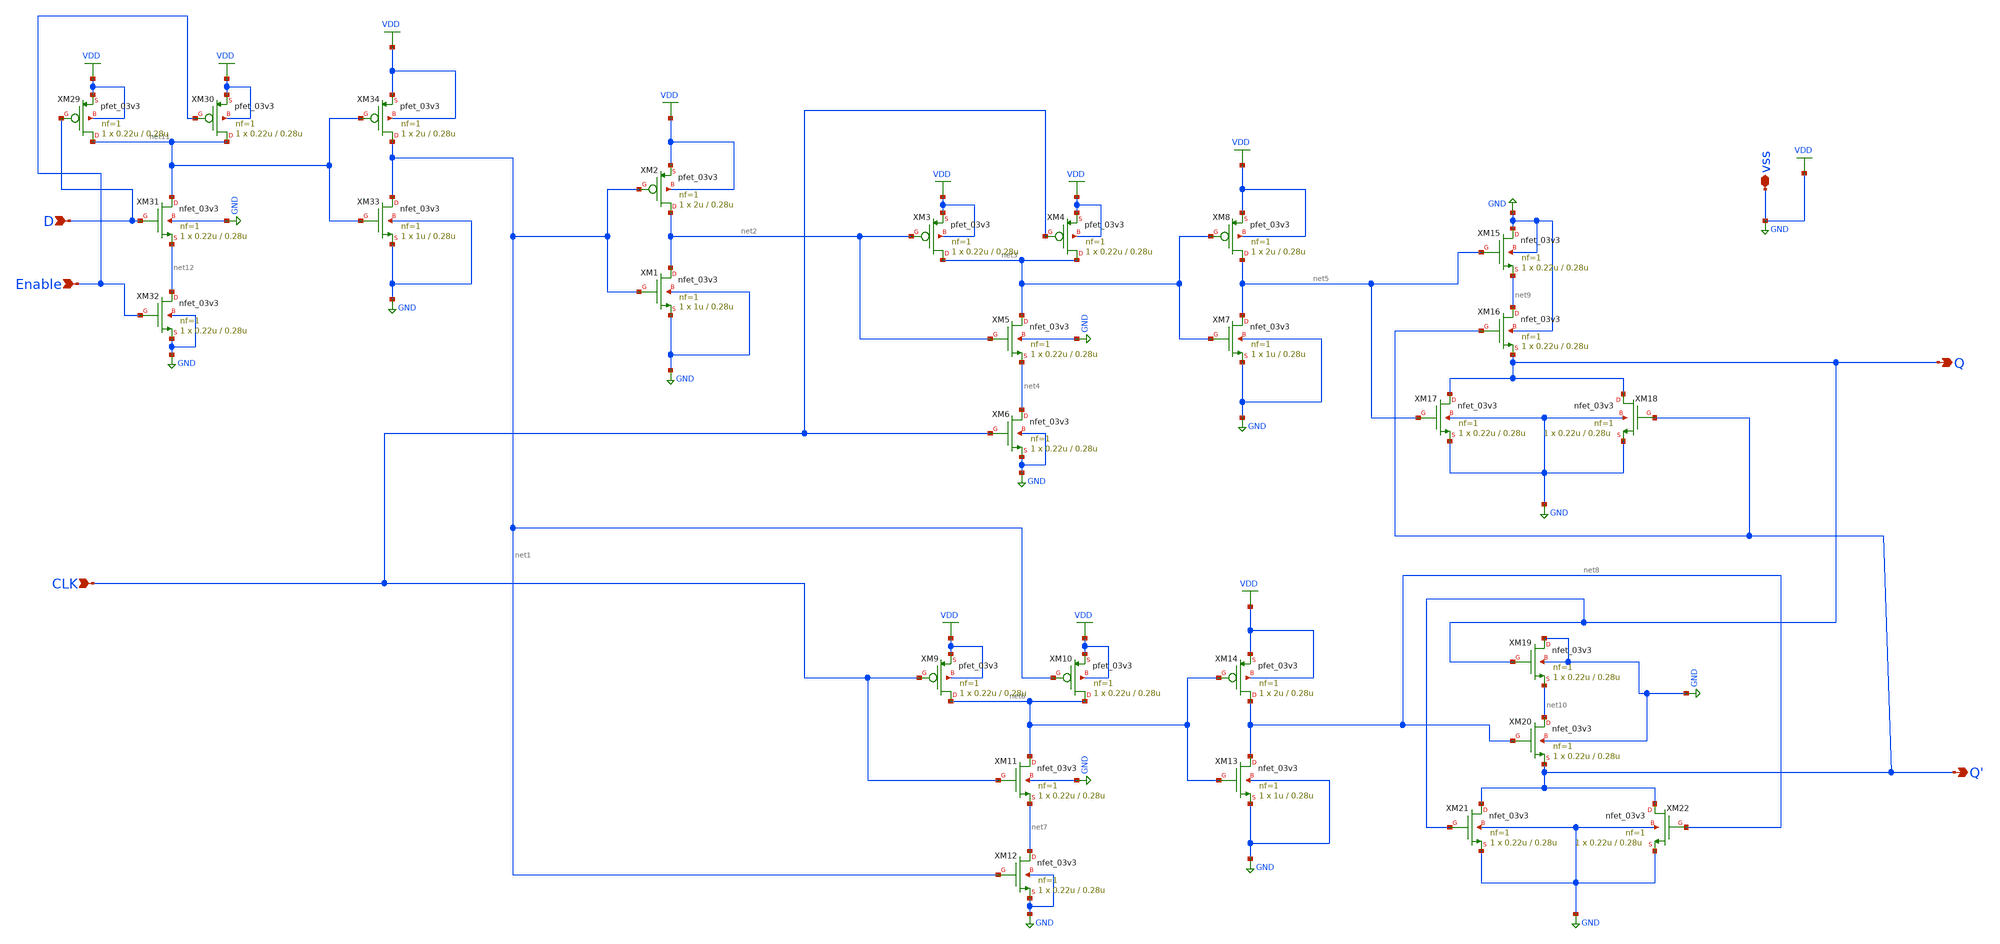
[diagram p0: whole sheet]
** sch_path: designs/DFFE/DFFE.sch
**.subckt DFFE D Enable Q Q' vss CLK
*.ipin D
*.ipin Enable
*.opin Q
*.opin Q'
*.iopin vss
*.ipin CLK
XM1 net2 net1 GND GND nfet_03v3 L=0.28u W=1u nf=1 ad='int((nf+1)/2) * W/nf * 0.18u' as='int((nf+2)/2) * W/nf * 0.18u'
+ pd='2*int((nf+1)/2) * (W/nf + 0.18u)' ps='2*int((nf+2)/2) * (W/nf + 0.18u)' nrd='0.18u / W' nrs='0.18u / W'
+ sa=0 sb=0 sd=0 m=1
XM2 net2 net1 VDD VDD pfet_03v3 L=0.28u W=2u nf=1 ad='int((nf+1)/2) * W/nf * 0.18u' as='int((nf+2)/2) * W/nf * 0.18u'
+ pd='2*int((nf+1)/2) * (W/nf + 0.18u)' ps='2*int((nf+2)/2) * (W/nf + 0.18u)' nrd='0.18u / W' nrs='0.18u / W'
+ sa=0 sb=0 sd=0 m=1
XM3 net3 net2 VDD VDD pfet_03v3 L=0.28u W=0.22u nf=1 ad='int((nf+1)/2) * W/nf * 0.18u' as='int((nf+2)/2) * W/nf * 0.18u'
+ pd='2*int((nf+1)/2) * (W/nf + 0.18u)' ps='2*int((nf+2)/2) * (W/nf + 0.18u)' nrd='0.18u / W' nrs='0.18u / W'
+ sa=0 sb=0 sd=0 m=1
XM4 net3 CLK VDD VDD pfet_03v3 L=0.28u W=0.22u nf=1 ad='int((nf+1)/2) * W/nf * 0.18u' as='int((nf+2)/2) * W/nf * 0.18u'
+ pd='2*int((nf+1)/2) * (W/nf + 0.18u)' ps='2*int((nf+2)/2) * (W/nf + 0.18u)' nrd='0.18u / W' nrs='0.18u / W'
+ sa=0 sb=0 sd=0 m=1
XM5 net3 net2 net4 GND nfet_03v3 L=0.28u W=0.22u nf=1 ad='int((nf+1)/2) * W/nf * 0.18u' as='int((nf+2)/2) * W/nf * 0.18u'
+ pd='2*int((nf+1)/2) * (W/nf + 0.18u)' ps='2*int((nf+2)/2) * (W/nf + 0.18u)' nrd='0.18u / W' nrs='0.18u / W'
+ sa=0 sb=0 sd=0 m=1
XM6 net4 CLK GND GND nfet_03v3 L=0.28u W=0.22u nf=1 ad='int((nf+1)/2) * W/nf * 0.18u' as='int((nf+2)/2) * W/nf * 0.18u'
+ pd='2*int((nf+1)/2) * (W/nf + 0.18u)' ps='2*int((nf+2)/2) * (W/nf + 0.18u)' nrd='0.18u / W' nrs='0.18u / W'
+ sa=0 sb=0 sd=0 m=1
XM7 net5 net3 GND GND nfet_03v3 L=0.28u W=1u nf=1 ad='int((nf+1)/2) * W/nf * 0.18u' as='int((nf+2)/2) * W/nf * 0.18u'
+ pd='2*int((nf+1)/2) * (W/nf + 0.18u)' ps='2*int((nf+2)/2) * (W/nf + 0.18u)' nrd='0.18u / W' nrs='0.18u / W'
+ sa=0 sb=0 sd=0 m=1
XM8 net5 net3 VDD VDD pfet_03v3 L=0.28u W=2u nf=1 ad='int((nf+1)/2) * W/nf * 0.18u' as='int((nf+2)/2) * W/nf * 0.18u'
+ pd='2*int((nf+1)/2) * (W/nf + 0.18u)' ps='2*int((nf+2)/2) * (W/nf + 0.18u)' nrd='0.18u / W' nrs='0.18u / W'
+ sa=0 sb=0 sd=0 m=1
XM9 net6 CLK VDD VDD pfet_03v3 L=0.28u W=0.22u nf=1 ad='int((nf+1)/2) * W/nf * 0.18u' as='int((nf+2)/2) * W/nf * 0.18u'
+ pd='2*int((nf+1)/2) * (W/nf + 0.18u)' ps='2*int((nf+2)/2) * (W/nf + 0.18u)' nrd='0.18u / W' nrs='0.18u / W'
+ sa=0 sb=0 sd=0 m=1
XM10 net6 net1 VDD VDD pfet_03v3 L=0.28u W=0.22u nf=1 ad='int((nf+1)/2) * W/nf * 0.18u' as='int((nf+2)/2) * W/nf * 0.18u'
+ pd='2*int((nf+1)/2) * (W/nf + 0.18u)' ps='2*int((nf+2)/2) * (W/nf + 0.18u)' nrd='0.18u / W' nrs='0.18u / W'
+ sa=0 sb=0 sd=0 m=1
XM11 net6 CLK net7 GND nfet_03v3 L=0.28u W=0.22u nf=1 ad='int((nf+1)/2) * W/nf * 0.18u' as='int((nf+2)/2) * W/nf * 0.18u'
+ pd='2*int((nf+1)/2) * (W/nf + 0.18u)' ps='2*int((nf+2)/2) * (W/nf + 0.18u)' nrd='0.18u / W' nrs='0.18u / W'
+ sa=0 sb=0 sd=0 m=1
XM12 net7 net1 GND GND nfet_03v3 L=0.28u W=0.22u nf=1 ad='int((nf+1)/2) * W/nf * 0.18u' as='int((nf+2)/2) * W/nf * 0.18u'
+ pd='2*int((nf+1)/2) * (W/nf + 0.18u)' ps='2*int((nf+2)/2) * (W/nf + 0.18u)' nrd='0.18u / W' nrs='0.18u / W'
+ sa=0 sb=0 sd=0 m=1
XM13 net8 net6 GND GND nfet_03v3 L=0.28u W=1u nf=1 ad='int((nf+1)/2) * W/nf * 0.18u' as='int((nf+2)/2) * W/nf * 0.18u'
+ pd='2*int((nf+1)/2) * (W/nf + 0.18u)' ps='2*int((nf+2)/2) * (W/nf + 0.18u)' nrd='0.18u / W' nrs='0.18u / W'
+ sa=0 sb=0 sd=0 m=1
XM14 net8 net6 VDD VDD pfet_03v3 L=0.28u W=2u nf=1 ad='int((nf+1)/2) * W/nf * 0.18u' as='int((nf+2)/2) * W/nf * 0.18u'
+ pd='2*int((nf+1)/2) * (W/nf + 0.18u)' ps='2*int((nf+2)/2) * (W/nf + 0.18u)' nrd='0.18u / W' nrs='0.18u / W'
+ sa=0 sb=0 sd=0 m=1
XM15 GND net5 net9 GND nfet_03v3 L=0.28u W=0.22u nf=1 ad='int((nf+1)/2) * W/nf * 0.18u' as='int((nf+2)/2) * W/nf * 0.18u'
+ pd='2*int((nf+1)/2) * (W/nf + 0.18u)' ps='2*int((nf+2)/2) * (W/nf + 0.18u)' nrd='0.18u / W' nrs='0.18u / W'
+ sa=0 sb=0 sd=0 m=1
XM16 net9 Q' Q GND nfet_03v3 L=0.28u W=0.22u nf=1 ad='int((nf+1)/2) * W/nf * 0.18u' as='int((nf+2)/2)
+ * W/nf * 0.18u' pd='2*int((nf+1)/2) * (W/nf + 0.18u)' ps='2*int((nf+2)/2) * (W/nf + 0.18u)' nrd='0.18u
+ / W' nrs='0.18u / W' sa=0 sb=0 sd=0 m=1
XM17 Q net5 GND GND nfet_03v3 L=0.28u W=0.22u nf=1 ad='int((nf+1)/2) * W/nf * 0.18u' as='int((nf+2)/2)
+ * W/nf * 0.18u' pd='2*int((nf+1)/2) * (W/nf + 0.18u)' ps='2*int((nf+2)/2) * (W/nf + 0.18u)' nrd='0.18u
+ / W' nrs='0.18u / W' sa=0 sb=0 sd=0 m=1
XM18 Q Q' GND GND nfet_03v3 L=0.28u W=0.22u nf=1 ad='int((nf+1)/2) * W/nf * 0.18u' as='int((nf+2)/2) * W/nf * 0.18u'
+ pd='2*int((nf+1)/2) * (W/nf + 0.18u)' ps='2*int((nf+2)/2) * (W/nf + 0.18u)' nrd='0.18u / W' nrs='0.18u / W'
+ sa=0 sb=0 sd=0 m=1
XM19 GND Q net10 GND nfet_03v3 L=0.28u W=0.22u nf=1 ad='int((nf+1)/2) * W/nf * 0.18u' as='int((nf+2)/2) * W/nf * 0.18u'
+ pd='2*int((nf+1)/2) * (W/nf + 0.18u)' ps='2*int((nf+2)/2) * (W/nf + 0.18u)' nrd='0.18u / W' nrs='0.18u / W'
+ sa=0 sb=0 sd=0 m=1
XM20 net10 net8 Q' GND nfet_03v3 L=0.28u W=0.22u nf=1 ad='int((nf+1)/2) * W/nf * 0.18u' as='int((nf+2)/2)
+ * W/nf * 0.18u' pd='2*int((nf+1)/2) * (W/nf + 0.18u)' ps='2*int((nf+2)/2) * (W/nf + 0.18u)' nrd='0.18u
+ / W' nrs='0.18u / W' sa=0 sb=0 sd=0 m=1
XM21 Q' Q GND GND nfet_03v3 L=0.28u W=0.22u nf=1 ad='int((nf+1)/2) * W/nf * 0.18u' as='int((nf+2)/2) * W/nf * 0.18u'
+ pd='2*int((nf+1)/2) * (W/nf + 0.18u)' ps='2*int((nf+2)/2) * (W/nf + 0.18u)' nrd='0.18u / W' nrs='0.18u / W'
+ sa=0 sb=0 sd=0 m=1
XM22 Q' net8 GND GND nfet_03v3 L=0.28u W=0.22u nf=1 ad='int((nf+1)/2) * W/nf * 0.18u' as='int((nf+2)/2)
+ * W/nf * 0.18u' pd='2*int((nf+1)/2) * (W/nf + 0.18u)' ps='2*int((nf+2)/2) * (W/nf + 0.18u)' nrd='0.18u
+ / W' nrs='0.18u / W' sa=0 sb=0 sd=0 m=1
XM29 net11 D VDD VDD pfet_03v3 L=0.28u W=0.22u nf=1 ad='int((nf+1)/2) * W/nf * 0.18u' as='int((nf+2)/2)
+ * W/nf * 0.18u' pd='2*int((nf+1)/2) * (W/nf + 0.18u)' ps='2*int((nf+2)/2) * (W/nf + 0.18u)' nrd='0.18u
+ / W' nrs='0.18u / W' sa=0 sb=0 sd=0 m=1
XM30 net11 Enable VDD VDD pfet_03v3 L=0.28u W=0.22u nf=1 ad='int((nf+1)/2) * W/nf * 0.18u' as='int((nf+2)/2)
+ * W/nf * 0.18u' pd='2*int((nf+1)/2) * (W/nf + 0.18u)' ps='2*int((nf+2)/2) * (W/nf + 0.18u)' nrd='0.18u
+ / W' nrs='0.18u / W' sa=0 sb=0 sd=0 m=1
XM31 net11 D net12 GND nfet_03v3 L=0.28u W=0.22u nf=1 ad='int((nf+1)/2) * W/nf * 0.18u' as='int((nf+2)/2)
+ * W/nf * 0.18u' pd='2*int((nf+1)/2) * (W/nf + 0.18u)' ps='2*int((nf+2)/2) * (W/nf + 0.18u)' nrd='0.18u
+ / W' nrs='0.18u / W' sa=0 sb=0 sd=0 m=1
XM32 net12 Enable GND GND nfet_03v3 L=0.28u W=0.22u nf=1 ad='int((nf+1)/2) * W/nf * 0.18u' as='int((nf+2)/2)
+ * W/nf * 0.18u' pd='2*int((nf+1)/2) * (W/nf + 0.18u)' ps='2*int((nf+2)/2) * (W/nf + 0.18u)' nrd='0.18u
+ / W' nrs='0.18u / W' sa=0 sb=0 sd=0 m=1
XM33 net1 net11 GND GND nfet_03v3 L=0.28u W=1u nf=1 ad='int((nf+1)/2) * W/nf * 0.18u' as='int((nf+2)/2)
+ * W/nf * 0.18u' pd='2*int((nf+1)/2) * (W/nf + 0.18u)' ps='2*int((nf+2)/2) * (W/nf + 0.18u)' nrd='0.18u
+ / W' nrs='0.18u / W' sa=0 sb=0 sd=0 m=1
XM34 net1 net11 VDD VDD pfet_03v3 L=0.28u W=2u nf=1 ad='int((nf+1)/2) * W/nf * 0.18u' as='int((nf+2)/2)
+ * W/nf * 0.18u' pd='2*int((nf+1)/2) * (W/nf + 0.18u)' ps='2*int((nf+2)/2) * (W/nf + 0.18u)' nrd='0.18u
+ / W' nrs='0.18u / W' sa=0 sb=0 sd=0 m=1
**.ends
.GLOBAL VDD
.GLOBAL GND
.end
